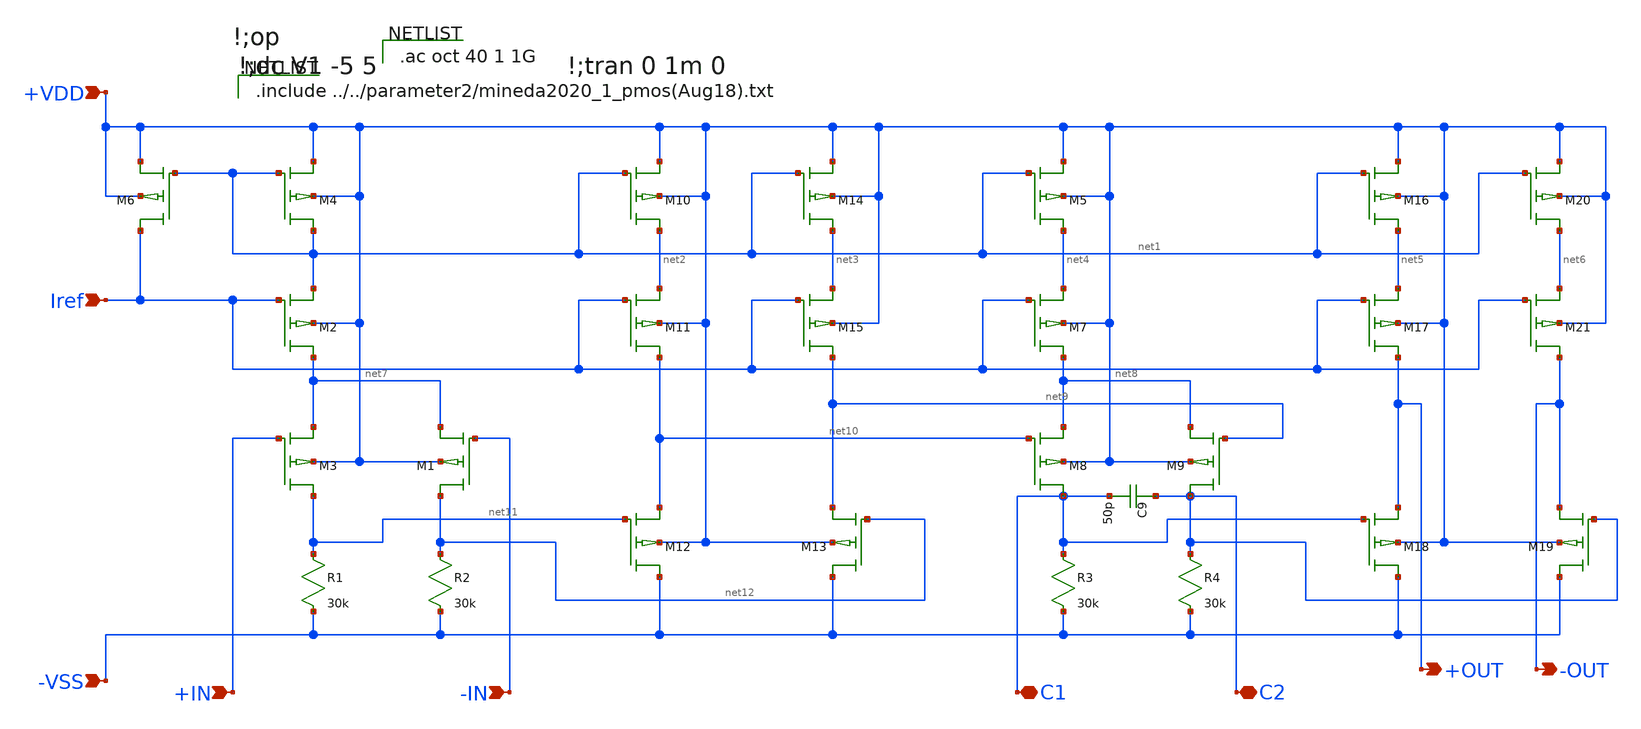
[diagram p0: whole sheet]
** sch_path: DiffAmp.sch
**.subckt DiffAmp -OUT +OUT +VDD -VSS Iref +IN -IN C1 C2
*.opin -OUT
*.opin +OUT
*.ipin +VDD
*.ipin -VSS
*.ipin Iref
*.ipin +IN
*.ipin -IN
*.iopin C1
*.iopin C2
M6 Iref net1 +VDD +VDD YSS_PMOS w=280u l=14u as=3.92n ps=308u ad=3.92n pd=308u m=1
M2 net7 Iref net1 +VDD YSS_PMOS w=84u l=14u as=1.176n ps=112u ad=1.176n pd=112u m=1
M3 net11 +IN net7 +VDD YSS_PMOS w=200u l=10u as=2.0n ps=220u ad=2.0n pd=220u m=1
R1 net11 -VSS 30k m=1
R2 net12 -VSS 30k m=1
R3 C1 -VSS 30k m=1
R4 C2 -VSS 30k m=1
M4 net1 net1 +VDD +VDD YSS_PMOS w=280u l=14u as=3.92n ps=308u ad=3.92n pd=308u m=1
M5 net4 net1 +VDD +VDD YSS_PMOS w=280u l=14u as=3.92n ps=308u ad=3.92n pd=308u m=1
M7 net8 Iref net4 +VDD YSS_PMOS w=84u l=14u as=1.176n ps=112u ad=1.176n pd=112u m=1
M8 C1 net10 net8 +VDD YSS_PMOS w=200u l=10u as=2.0n ps=220u ad=2.0n pd=220u m=1
M1 net12 -IN net7 +VDD YSS_PMOS w=200u l=10u as=2.0n ps=220u ad=2.0n pd=220u m=1
M9 C2 net9 net8 +VDD YSS_PMOS w=200u l=10u as=2.0n ps=220u ad=2.0n pd=220u m=1
M10 net2 net1 +VDD +VDD YSS_PMOS w=280u l=14u as=3.92n ps=308u ad=3.92n pd=308u m=1
M11 net10 Iref net2 +VDD YSS_PMOS w=84u l=14u as=1.176n ps=112u ad=1.176n pd=112u m=1
M12 -VSS net11 net10 +VDD YSS_PMOS w=200u l=10u as=2.0n ps=220u ad=2.0n pd=220u m=1
M13 -VSS net12 net9 +VDD YSS_PMOS w=200u l=10u as=2.0n ps=220u ad=2.0n pd=220u m=1
M14 net3 net1 +VDD +VDD YSS_PMOS w=280u l=14u as=3.92n ps=308u ad=3.92n pd=308u m=1
M15 net9 Iref net3 +VDD YSS_PMOS w=84u l=14u as=1.176n ps=112u ad=1.176n pd=112u m=1
M16 net5 net1 +VDD +VDD YSS_PMOS w=280u l=14u as=3.92n ps=308u ad=3.92n pd=308u m=4
M17 +OUT Iref net5 +VDD YSS_PMOS w=84u l=14u as=1.176n ps=112u ad=1.176n pd=112u m=4
M18 -VSS C1 +OUT +VDD YSS_PMOS w=200u l=10u as=2.0n ps=220u ad=2.0n pd=220u m=4
M19 -VSS C2 -OUT +VDD YSS_PMOS w=200u l=10u as=2.0n ps=220u ad=2.0n pd=220u m=4
M20 net6 net1 +VDD +VDD YSS_PMOS w=280u l=14u as=3.92n ps=308u ad=3.92n pd=308u m=4
M21 -OUT Iref net6 +VDD YSS_PMOS w=84u l=14u as=1.176n ps=112u ad=1.176n pd=112u m=4
C9 C2 C1 50p m=1
**** begin user architecture code

.include ../../parameter2/mineda2020_1_pmos(Aug18).txt


.ac oct 40 1 1G

**** end user architecture code
**.ends
.end
